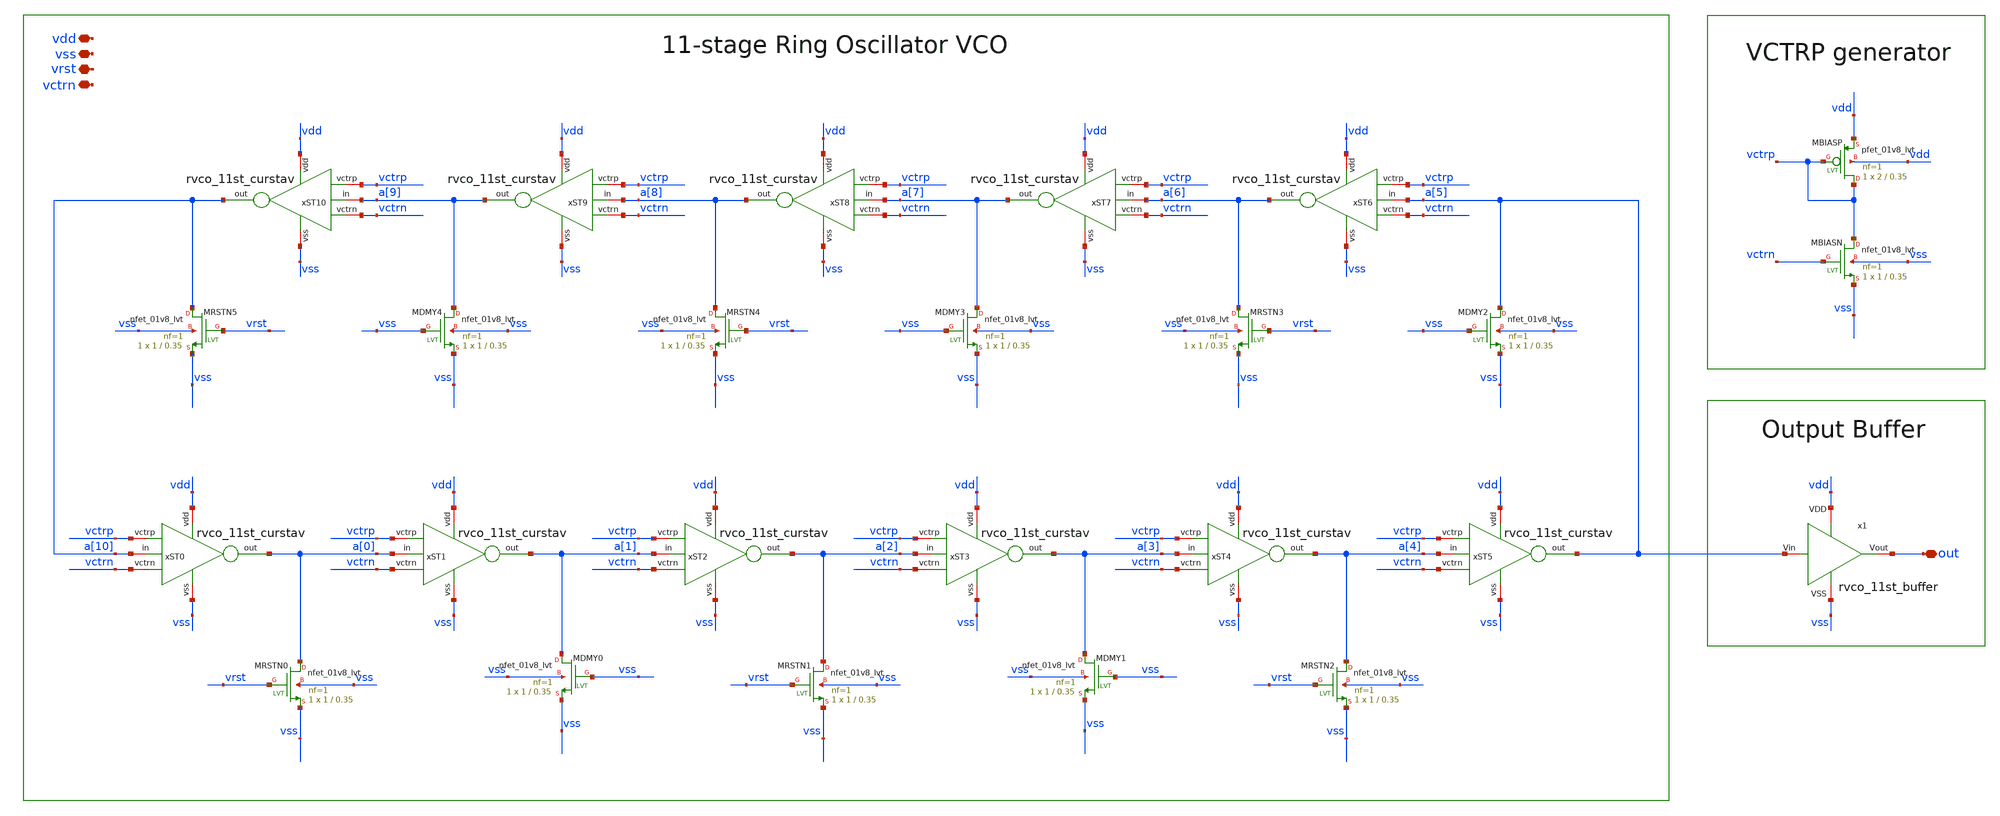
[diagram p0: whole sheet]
** sch_path: xschem/rvco_11st_oscillator.sch
**.subckt rvco_11st_oscillator vdd vctrn vss vrst out
*.iopin vdd
*.iopin vctrn
*.iopin vss
*.iopin vrst
*.iopin out
XMRSTN0 a[0] vrst vss vss sky130_fd_pr__nfet_01v8_lvt L=0.35 W=1 nf=1 ad='int((1 + 1)/2) * 1 / 1 * 0.29'
+ as='int((1 + 2)/2) * 1 / 1 * 0.29' pd='2*int((1 + 1)/2) * (1 / 1 + 0.29)' ps='2*int((1 + 2)/2) * (1 / 1 + 0.29)'
+ nrd='0.29 / 1 ' nrs='0.29 / 1 ' sa=0 sb=0 sd=0 mult=1 m=1
XMBIASN vctrp vctrn vss vss sky130_fd_pr__nfet_01v8_lvt L=0.35 W=1 nf=1 ad='int((1 + 1)/2) * 1 / 1 * 0.29'
+ as='int((1 + 2)/2) * 1 / 1 * 0.29' pd='2*int((1 + 1)/2) * (1 / 1 + 0.29)' ps='2*int((1 + 2)/2) * (1 / 1 + 0.29)'
+ nrd='0.29 / 1 ' nrs='0.29 / 1 ' sa=0 sb=0 sd=0 mult=1 m=1
XMBIASP vctrp vctrp vdd vdd sky130_fd_pr__pfet_01v8_lvt L=0.35 W=2 nf=1 ad='int((1 + 1)/2) * 2 / 1 * 0.29'
+ as='int((1 + 2)/2) * 2 / 1 * 0.29' pd='2*int((1 + 1)/2) * (2 / 1 + 0.29)' ps='2*int((1 + 2)/2) * (2 / 1 + 0.29)'
+ nrd='0.29 / 2 ' nrs='0.29 / 2 ' sa=0 sb=0 sd=0 mult=1 m=1
xST0 vdd a[0] a[10] vss vctrp vctrn rvco_11st_curstav
XMRSTN1 a[2] vrst vss vss sky130_fd_pr__nfet_01v8_lvt L=0.35 W=1 nf=1 ad='int((1 + 1)/2) * 1 / 1 * 0.29'
+ as='int((1 + 2)/2) * 1 / 1 * 0.29' pd='2*int((1 + 1)/2) * (1 / 1 + 0.29)' ps='2*int((1 + 2)/2) * (1 / 1 + 0.29)'
+ nrd='0.29 / 1 ' nrs='0.29 / 1 ' sa=0 sb=0 sd=0 mult=1 m=1
XMRSTN2 a[4] vrst vss vss sky130_fd_pr__nfet_01v8_lvt L=0.35 W=1 nf=1 ad='int((1 + 1)/2) * 1 / 1 * 0.29'
+ as='int((1 + 2)/2) * 1 / 1 * 0.29' pd='2*int((1 + 1)/2) * (1 / 1 + 0.29)' ps='2*int((1 + 2)/2) * (1 / 1 + 0.29)'
+ nrd='0.29 / 1 ' nrs='0.29 / 1 ' sa=0 sb=0 sd=0 mult=1 m=1
XMRSTN3 a[6] vrst vss vss sky130_fd_pr__nfet_01v8_lvt L=0.35 W=1 nf=1 ad='int((1 + 1)/2) * 1 / 1 * 0.29'
+ as='int((1 + 2)/2) * 1 / 1 * 0.29' pd='2*int((1 + 1)/2) * (1 / 1 + 0.29)' ps='2*int((1 + 2)/2) * (1 / 1 + 0.29)'
+ nrd='0.29 / 1 ' nrs='0.29 / 1 ' sa=0 sb=0 sd=0 mult=1 m=1
XMRSTN4 a[8] vrst vss vss sky130_fd_pr__nfet_01v8_lvt L=0.35 W=1 nf=1 ad='int((1 + 1)/2) * 1 / 1 * 0.29'
+ as='int((1 + 2)/2) * 1 / 1 * 0.29' pd='2*int((1 + 1)/2) * (1 / 1 + 0.29)' ps='2*int((1 + 2)/2) * (1 / 1 + 0.29)'
+ nrd='0.29 / 1 ' nrs='0.29 / 1 ' sa=0 sb=0 sd=0 mult=1 m=1
XMRSTN5 a[10] vrst vss vss sky130_fd_pr__nfet_01v8_lvt L=0.35 W=1 nf=1 ad='int((1 + 1)/2) * 1 / 1 * 0.29'
+ as='int((1 + 2)/2) * 1 / 1 * 0.29' pd='2*int((1 + 1)/2) * (1 / 1 + 0.29)' ps='2*int((1 + 2)/2) * (1 / 1 + 0.29)'
+ nrd='0.29 / 1 ' nrs='0.29 / 1 ' sa=0 sb=0 sd=0 mult=1 m=1
XMDMY4 a[9] vss vss vss sky130_fd_pr__nfet_01v8_lvt L=0.35 W=1 nf=1 ad='int((1 + 1)/2) * 1 / 1 * 0.29'
+ as='int((1 + 2)/2) * 1 / 1 * 0.29' pd='2*int((1 + 1)/2) * (1 / 1 + 0.29)' ps='2*int((1 + 2)/2) * (1 / 1 + 0.29)'
+ nrd='0.29 / 1 ' nrs='0.29 / 1 ' sa=0 sb=0 sd=0 mult=1 m=1
XMDMY3 a[7] vss vss vss sky130_fd_pr__nfet_01v8_lvt L=0.35 W=1 nf=1 ad='int((1 + 1)/2) * 1 / 1 * 0.29'
+ as='int((1 + 2)/2) * 1 / 1 * 0.29' pd='2*int((1 + 1)/2) * (1 / 1 + 0.29)' ps='2*int((1 + 2)/2) * (1 / 1 + 0.29)'
+ nrd='0.29 / 1 ' nrs='0.29 / 1 ' sa=0 sb=0 sd=0 mult=1 m=1
XMDMY2 a[5] vss vss vss sky130_fd_pr__nfet_01v8_lvt L=0.35 W=1 nf=1 ad='int((1 + 1)/2) * 1 / 1 * 0.29'
+ as='int((1 + 2)/2) * 1 / 1 * 0.29' pd='2*int((1 + 1)/2) * (1 / 1 + 0.29)' ps='2*int((1 + 2)/2) * (1 / 1 + 0.29)'
+ nrd='0.29 / 1 ' nrs='0.29 / 1 ' sa=0 sb=0 sd=0 mult=1 m=1
XMDMY0 a[1] vss vss vss sky130_fd_pr__nfet_01v8_lvt L=0.35 W=1 nf=1 ad='int((1 + 1)/2) * 1 / 1 * 0.29'
+ as='int((1 + 2)/2) * 1 / 1 * 0.29' pd='2*int((1 + 1)/2) * (1 / 1 + 0.29)' ps='2*int((1 + 2)/2) * (1 / 1 + 0.29)'
+ nrd='0.29 / 1 ' nrs='0.29 / 1 ' sa=0 sb=0 sd=0 mult=1 m=1
XMDMY1 a[3] vss vss vss sky130_fd_pr__nfet_01v8_lvt L=0.35 W=1 nf=1 ad='int((1 + 1)/2) * 1 / 1 * 0.29'
+ as='int((1 + 2)/2) * 1 / 1 * 0.29' pd='2*int((1 + 1)/2) * (1 / 1 + 0.29)' ps='2*int((1 + 2)/2) * (1 / 1 + 0.29)'
+ nrd='0.29 / 1 ' nrs='0.29 / 1 ' sa=0 sb=0 sd=0 mult=1 m=1
x1 vdd vss a[5] out rvco_11st_buffer
xST1 vdd a[1] a[0] vss vctrp vctrn rvco_11st_curstav
xST2 vdd a[2] a[1] vss vctrp vctrn rvco_11st_curstav
xST3 vdd a[3] a[2] vss vctrp vctrn rvco_11st_curstav
xST4 vdd a[4] a[3] vss vctrp vctrn rvco_11st_curstav
xST5 vdd a[5] a[4] vss vctrp vctrn rvco_11st_curstav
xST6 vdd a[6] a[5] vss vctrp vctrn rvco_11st_curstav
xST7 vdd a[7] a[6] vss vctrp vctrn rvco_11st_curstav
xST8 vdd a[8] a[7] vss vctrp vctrn rvco_11st_curstav
xST9 vdd a[9] a[8] vss vctrp vctrn rvco_11st_curstav
xST10 vdd a[10] a[9] vss vctrp vctrn rvco_11st_curstav
**.ends

* expanding   symbol:  rvco_11st_curstav.sym # of pins=6
** sym_path: xschem/rvco_11st_curstav.sym
** sch_path: xschem/rvco_11st_curstav.sch
.subckt rvco_11st_curstav vdd out in vss vctrp vctrn
*.iopin vctrp
*.iopin vctrn
*.iopin vdd
*.iopin vss
*.ipin in
*.opin out
XMIP out in XP vdd sky130_fd_pr__pfet_01v8_lvt L=0.35 W=2 nf=1 ad='int((1 + 1)/2) * 2 / 1 * 0.29' as='int((1 + 2)/2) * 2 / 1 * 0.29'
+ pd='2*int((1 + 1)/2) * (2 / 1 + 0.29)' ps='2*int((1 + 2)/2) * (2 / 1 + 0.29)' nrd='0.29 / 2 ' nrs='0.29 / 2 '
+ sa=0 sb=0 sd=0 mult=1 m=1
XMCP XP vctrp vdd vdd sky130_fd_pr__pfet_01v8_lvt L=0.35 W=2 nf=1 ad='int((1 + 1)/2) * 2 / 1 * 0.29'
+ as='int((1 + 2)/2) * 2 / 1 * 0.29' pd='2*int((1 + 1)/2) * (2 / 1 + 0.29)' ps='2*int((1 + 2)/2) * (2 / 1 + 0.29)'
+ nrd='0.29 / 2 ' nrs='0.29 / 2 ' sa=0 sb=0 sd=0 mult=1 m=1
XMIN XN in out vss sky130_fd_pr__nfet_01v8_lvt L=0.35 W=1 nf=1 ad='int((1 + 1)/2) * 1 / 1 * 0.29' as='int((1 + 2)/2) * 1 / 1 * 0.29'
+ pd='2*int((1 + 1)/2) * (1 / 1 + 0.29)' ps='2*int((1 + 2)/2) * (1 / 1 + 0.29)' nrd='0.29 / 1 ' nrs='0.29 / 1 '
+ sa=0 sb=0 sd=0 mult=1 m=1
XMCN vss vctrn XN vss sky130_fd_pr__nfet_01v8_lvt L=0.35 W=1 nf=1 ad='int((1 + 1)/2) * 1 / 1 * 0.29'
+ as='int((1 + 2)/2) * 1 / 1 * 0.29' pd='2*int((1 + 1)/2) * (1 / 1 + 0.29)' ps='2*int((1 + 2)/2) * (1 / 1 + 0.29)'
+ nrd='0.29 / 1 ' nrs='0.29 / 1 ' sa=0 sb=0 sd=0 mult=1 m=1
XMDMYP1 XP vdd vdd vdd sky130_fd_pr__pfet_01v8_lvt L=0.35 W=2 nf=1 ad='int((1 + 1)/2) * 2 / 1 * 0.29'
+ as='int((1 + 2)/2) * 2 / 1 * 0.29' pd='2*int((1 + 1)/2) * (2 / 1 + 0.29)' ps='2*int((1 + 2)/2) * (2 / 1 + 0.29)'
+ nrd='0.29 / 2 ' nrs='0.29 / 2 ' sa=0 sb=0 sd=0 mult=1 m=1
XMDMYP2 vdd vdd vdd vdd sky130_fd_pr__pfet_01v8_lvt L=0.35 W=2 nf=1 ad='int((1 + 1)/2) * 2 / 1 * 0.29'
+ as='int((1 + 2)/2) * 2 / 1 * 0.29' pd='2*int((1 + 1)/2) * (2 / 1 + 0.29)' ps='2*int((1 + 2)/2) * (2 / 1 + 0.29)'
+ nrd='0.29 / 2 ' nrs='0.29 / 2 ' sa=0 sb=0 sd=0 mult=1 m=1
XMDMYN1 XN vss vss vss sky130_fd_pr__nfet_01v8_lvt L=0.35 W=1 nf=1 ad='int((1 + 1)/2) * 1 / 1 * 0.29'
+ as='int((1 + 2)/2) * 1 / 1 * 0.29' pd='2*int((1 + 1)/2) * (1 / 1 + 0.29)' ps='2*int((1 + 2)/2) * (1 / 1 + 0.29)'
+ nrd='0.29 / 1 ' nrs='0.29 / 1 ' sa=0 sb=0 sd=0 mult=1 m=1
XMDMYN2 vss vss vss vss sky130_fd_pr__nfet_01v8_lvt L=0.35 W=1 nf=1 ad='int((1 + 1)/2) * 1 / 1 * 0.29'
+ as='int((1 + 2)/2) * 1 / 1 * 0.29' pd='2*int((1 + 1)/2) * (1 / 1 + 0.29)' ps='2*int((1 + 2)/2) * (1 / 1 + 0.29)'
+ nrd='0.29 / 1 ' nrs='0.29 / 1 ' sa=0 sb=0 sd=0 mult=1 m=1
.ends


* expanding   symbol:  rvco_11st_buffer.sym # of pins=4
** sym_path: xschem/rvco_11st_buffer.sym
** sch_path: xschem/rvco_11st_buffer.sch
.subckt rvco_11st_buffer VDD VSS Vin Vout
*.iopin VDD
*.iopin Vin
*.iopin Vout
*.iopin VSS
XMP1 X Vin VDD VDD sky130_fd_pr__pfet_01v8 L=0.15 W=2 nf=1 ad='int((nf+1)/2) * W/nf * 0.29' as='int((nf+2)/2) * W/nf * 0.29'
+ pd='2*int((nf+1)/2) * (W/nf + 0.29)' ps='2*int((nf+2)/2) * (W/nf + 0.29)' nrd='0.29 / W' nrs='0.29 / W'
+ sa=0 sb=0 sd=0 mult=1 m=1
XMP2 Vout X VDD VDD sky130_fd_pr__pfet_01v8 L=0.15 W=2 nf=1 ad='int((nf+1)/2) * W/nf * 0.29' as='int((nf+2)/2) * W/nf * 0.29'
+ pd='2*int((nf+1)/2) * (W/nf + 0.29)' ps='2*int((nf+2)/2) * (W/nf + 0.29)' nrd='0.29 / W' nrs='0.29 / W'
+ sa=0 sb=0 sd=0 mult=3 m=3
XMN1 X Vin VSS VSS sky130_fd_pr__nfet_01v8 L=0.15 W=1 nf=1 ad='int((1 + 1)/2) * 1 / 1 * 0.29' as='int((1 + 2)/2) * 1 / 1 * 0.29'
+ pd='2*int((1 + 1)/2) * (1 / 1 + 0.29)' ps='2*int((1 + 2)/2) * (1 / 1 + 0.29)' nrd='0.29 / 1 ' nrs='0.29 / 1 '
+ sa=0 sb=0 sd=0 mult=1 m=1
XMN2 Vout X VSS VSS sky130_fd_pr__nfet_01v8 L=0.15 W=1 nf=1 ad='int((1 + 1)/2) * 1 / 1 * 0.29' as='int((1 + 2)/2) * 1 / 1 * 0.29'
+ pd='2*int((1 + 1)/2) * (1 / 1 + 0.29)' ps='2*int((1 + 2)/2) * (1 / 1 + 0.29)' nrd='0.29 / 1 ' nrs='0.29 / 1 '
+ sa=0 sb=0 sd=0 mult=3 m=3
.ends

.end
